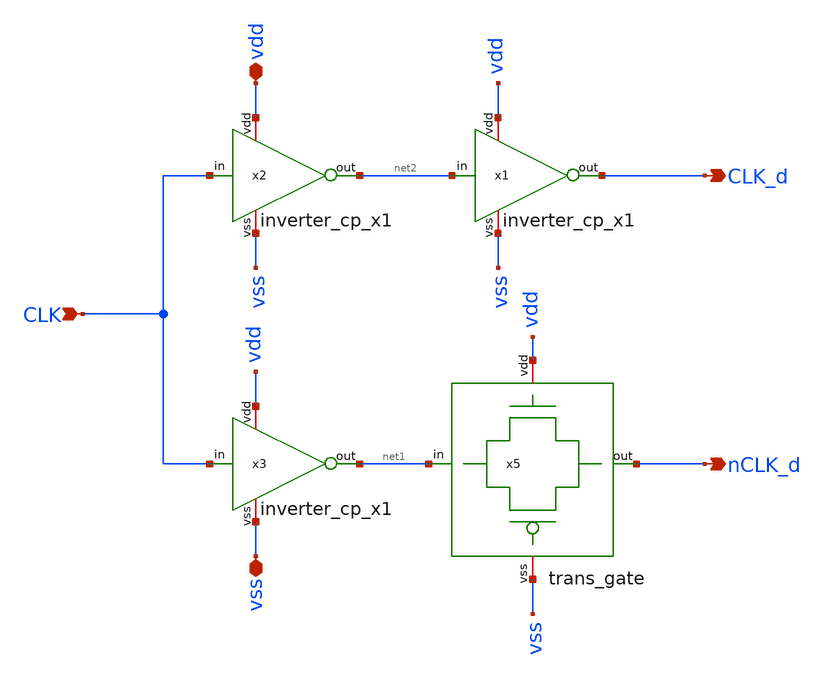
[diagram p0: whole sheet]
** sch_path: xschem/clock_inverter.sch
**.subckt clock_inverter CLK vdd vss nCLK_d CLK_d
*.ipin CLK
*.iopin vdd
*.iopin vss
*.opin nCLK_d
*.opin CLK_d
x5 vdd nCLK_d net1 vss trans_gate
x1 vdd CLK_d net2 vss inverter_cp_x1
x2 vdd net2 CLK vss inverter_cp_x1
x3 vdd net1 CLK vss inverter_cp_x1
**.ends
.end
